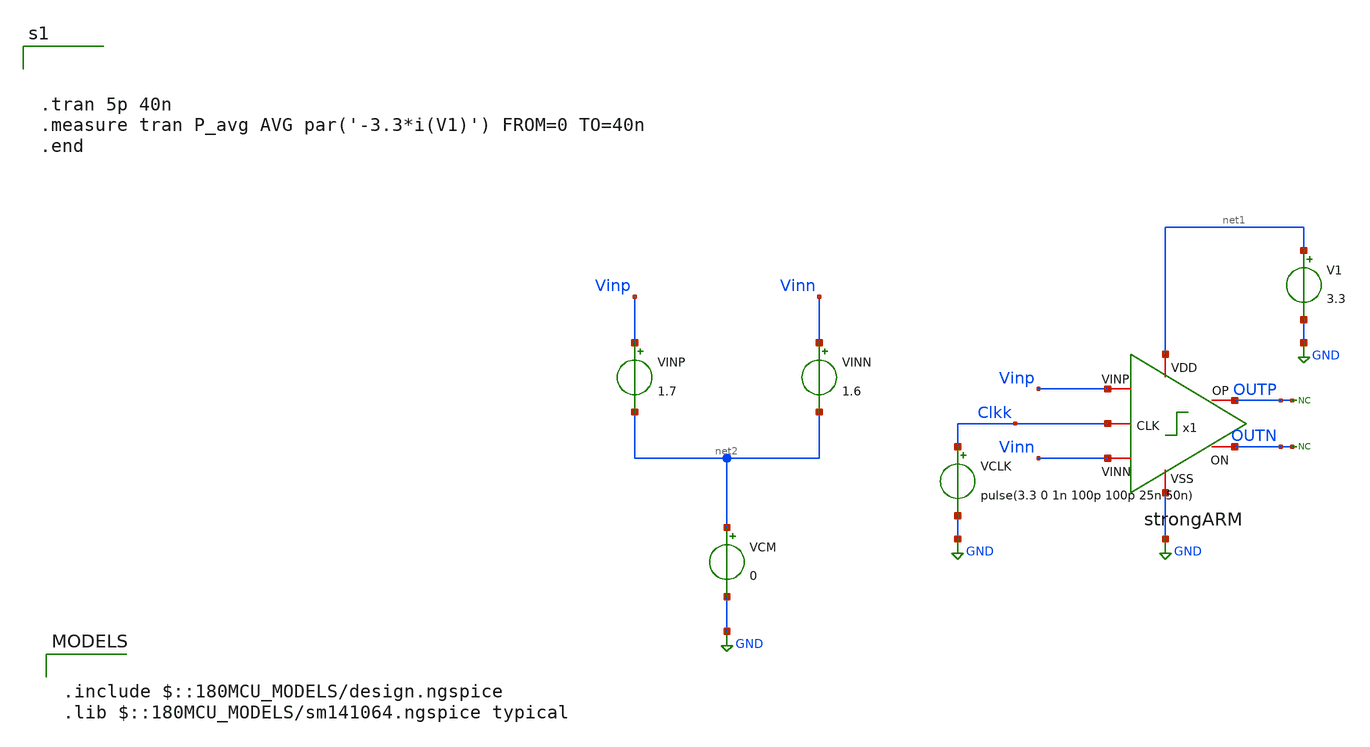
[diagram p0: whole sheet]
** sch_path: designs/sar_adc/comparator/comparador/xschem/Testbench/strongARM_tb.sch
**.subckt strongARM_tb
x1 Clkk net1 GND Vinn Vinp OUTP OUTN strongARM
V1 net1 GND 3.3
VCLK Clkk GND pulse(3.3 0 1n 100p 100p 25n 50n)
VCM net2 GND 0
VINP Vinp net2 1.7
VINN Vinn net2 1.6
* noconn OUTN
* noconn OUTP
**** begin user architecture code

.include $::180MCU_MODELS/design.ngspice
.lib $::180MCU_MODELS/sm141064.ngspice typical




.tran 5p 40n
.measure tran P_avg AVG par('-3.3*i(V1)') FROM=0 TO=40n
.end


**** end user architecture code
**.ends
.GLOBAL GND
.end
